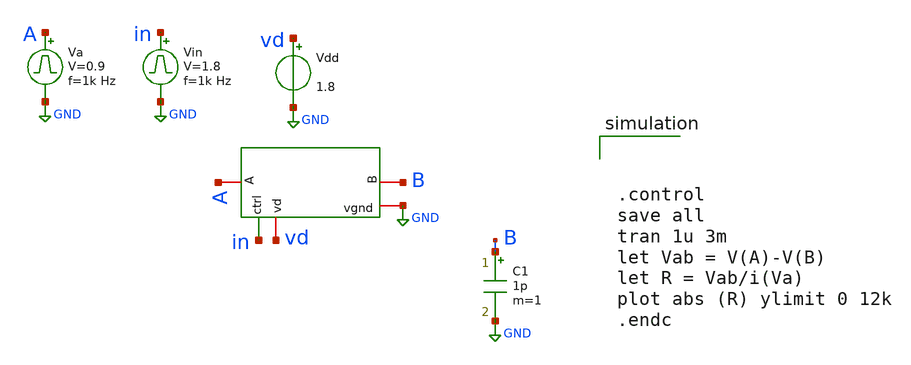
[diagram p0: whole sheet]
** sch_path: .Trash-1000/files/untitled-2.sch
**.subckt untitled-2
Vdd vd GND 1.8
Vin in GND pulse 0 1.8 '0.495/ 1k ' '0.01/1k ' '0.01/1k ' '0.49/1k ' '1/1k '
Va A GND pulse 0 0.9 '0.495/ 1k ' '0.01/1k ' '0.01/1k ' '0.49/1k ' '1/1k '
C1 B GND 1p m=1
x1 vd in GND A B tg
**** begin user architecture code

** opencircuitdesign pdks install
.lib $::SKYWATER_MODELS/sky130.lib.spice tt





.control
save all
tran 1u 3m
let Vab = V(A)-V(B)
let R = Vab/i(Va)
plot abs (R) ylimit 0 12k
.endc


**** end user architecture code
**.ends

* expanding   symbol:  /foss/designs/tg.sym # of pins=5
** sym_path: xschem/tg.sym
** sch_path: xschem/tg.sch
.subckt tg vd ctrl vgnd A B
*.iopin B
*.iopin A
*.iopin vgnd
*.iopin vd
*.ipin ctrl
x1 vd ctrl nctrl vgnd inverter
XM1 A ctrl B vgnd sky130_fd_pr__nfet_01v8 L=0.15 W=10 nf=1 ad='int((nf+1)/2) * W/nf * 0.29' as='int((nf+2)/2) * W/nf * 0.29'
+ pd='2*int((nf+1)/2) * (W/nf + 0.29)' ps='2*int((nf+2)/2) * (W/nf + 0.29)' nrd='0.29 / W' nrs='0.29 / W'
+ sa=0 sb=0 sd=0 mult=1 m=1
XM2 A nctrl B vd sky130_fd_pr__pfet_01v8 L=0.15 W=30 nf=1 ad='int((nf+1)/2) * W/nf * 0.29' as='int((nf+2)/2) * W/nf * 0.29'
+ pd='2*int((nf+1)/2) * (W/nf + 0.29)' ps='2*int((nf+2)/2) * (W/nf + 0.29)' nrd='0.29 / W' nrs='0.29 / W'
+ sa=0 sb=0 sd=0 mult=1 m=1
.ends


* expanding   symbol:  /foss/designs/inverter/xschem_files/inverter.sym # of pins=4
** sym_path: /foss/designs/inverter/xschem_files/inverter.sym
** sch_path: /foss/designs/inverter/xschem_files/inverter.sch
.subckt inverter vd in out gnd
*.ipin in
*.opin out
*.iopin vd
*.iopin gnd
XN0 out in gnd gnd sky130_fd_pr__nfet_01v8 L=0.15 W=1 nf=1 ad='int((nf+1)/2) * W/nf * 0.29' as='int((nf+2)/2) * W/nf * 0.29'
+ pd='2*int((nf+1)/2) * (W/nf + 0.29)' ps='2*int((nf+2)/2) * (W/nf + 0.29)' nrd='0.29 / W' nrs='0.29 / W'
+ sa=0 sb=0 sd=0 mult=1 m=1
XP0 out in vd vd sky130_fd_pr__pfet_01v8 L=0.15 W=3 nf=1 ad='int((nf+1)/2) * W/nf * 0.29' as='int((nf+2)/2) * W/nf * 0.29'
+ pd='2*int((nf+1)/2) * (W/nf + 0.29)' ps='2*int((nf+2)/2) * (W/nf + 0.29)' nrd='0.29 / W' nrs='0.29 / W'
+ sa=0 sb=0 sd=0 mult=1 m=1
.ends

.GLOBAL GND
.end
